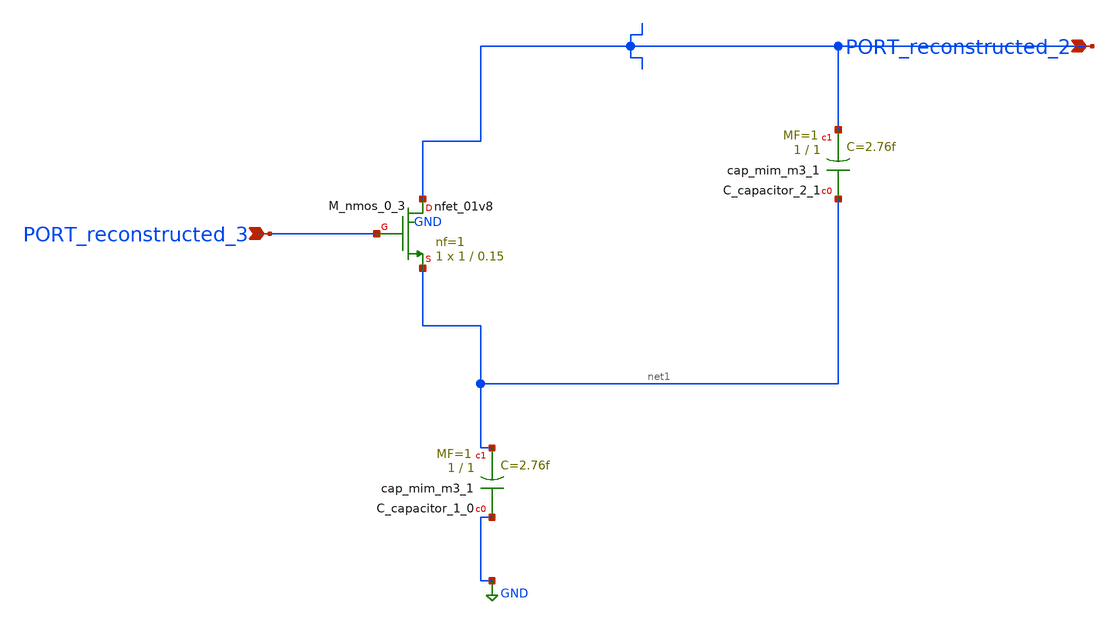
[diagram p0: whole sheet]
** sch_path: schematics/AMSNet/48.sch
**.subckt 48 PORT_reconstructed_3 PORT_reconstructed_2
*.ipin PORT_reconstructed_3
*.ipin PORT_reconstructed_2
XC_capacitor_1_0 GND net1 sky130_fd_pr__cap_mim_m3_1 W=1 L=1 MF=1 m=1
XC_capacitor_2_1 net1 PORT_reconstructed_2 sky130_fd_pr__cap_mim_m3_1 W=1 L=1 MF=1 m=1
XM_nmos_0_3 PORT_reconstructed_2 PORT_reconstructed_3 net1 GND sky130_fd_pr__nfet_01v8 L=0.15 W=1 nf=1
+ ad='int((1 + 1)/2) * 1 / 1 * 0.29' as='int((1 + 2)/2) * 1 / 1 * 0.29' pd='2*int((1 + 1)/2) * (1 / 1 + 0.29)'
+ ps='2*int((1 + 2)/2) * (1 / 1 + 0.29)' nrd='0.29 / 1 ' nrs='0.29 / 1 ' sa=0 sb=0 sd=0 mult=1 m=1
**.ends
.GLOBAL GND
.end
